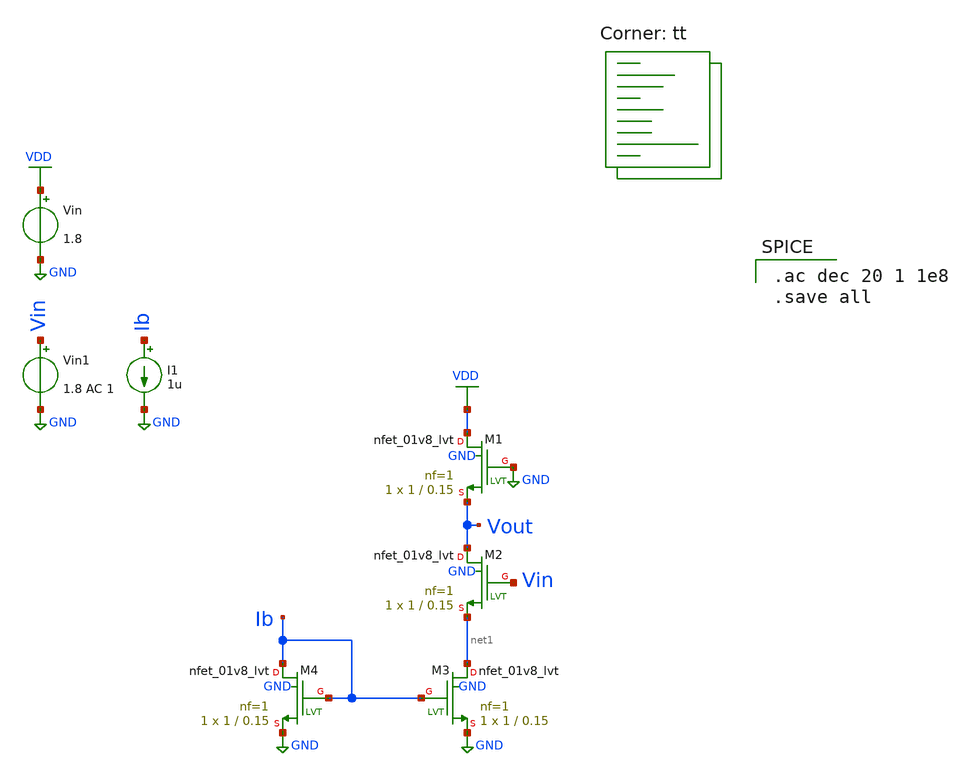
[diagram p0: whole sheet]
** sch_path: xschem/fvf_tb_loop.sch
**.subckt fvf_tb_loop
Vin VDD GND 1.8
Vin1 Vin GND 1.8 AC 1
I1 Ib GND 1u
XM1 VDD GND Vout GND sky130_fd_pr__nfet_01v8_lvt L=0.15 W=1 nf=1 ad='int((nf+1)/2) * W/nf * 0.29' as='int((nf+2)/2) * W/nf * 0.29'
+ pd='2*int((nf+1)/2) * (W/nf + 0.29)' ps='2*int((nf+2)/2) * (W/nf + 0.29)' nrd='0.29 / W' nrs='0.29 / W'
+ sa=0 sb=0 sd=0 mult=1 m=1
XM2 Vout Vin net1 GND sky130_fd_pr__nfet_01v8_lvt L=0.15 W=1 nf=1 ad='int((nf+1)/2) * W/nf * 0.29' as='int((nf+2)/2) * W/nf * 0.29'
+ pd='2*int((nf+1)/2) * (W/nf + 0.29)' ps='2*int((nf+2)/2) * (W/nf + 0.29)' nrd='0.29 / W' nrs='0.29 / W'
+ sa=0 sb=0 sd=0 mult=1 m=1
XM3 net1 Ib GND GND sky130_fd_pr__nfet_01v8_lvt L=0.15 W=1 nf=1 ad='int((nf+1)/2) * W/nf * 0.29' as='int((nf+2)/2) * W/nf * 0.29'
+ pd='2*int((nf+1)/2) * (W/nf + 0.29)' ps='2*int((nf+2)/2) * (W/nf + 0.29)' nrd='0.29 / W' nrs='0.29 / W'
+ sa=0 sb=0 sd=0 mult=1 m=1
XM4 Ib Ib GND GND sky130_fd_pr__nfet_01v8_lvt L=0.15 W=1 nf=1 ad='int((nf+1)/2) * W/nf * 0.29' as='int((nf+2)/2) * W/nf * 0.29'
+ pd='2*int((nf+1)/2) * (W/nf + 0.29)' ps='2*int((nf+2)/2) * (W/nf + 0.29)' nrd='0.29 / W' nrs='0.29 / W'
+ sa=0 sb=0 sd=0 mult=1 m=1
**** begin user architecture code
.lib $::SKYWATER_MODELS/sky130.lib.spice tt

.ac dec 20 1 1e8
.save all

**** end user architecture code
**.ends
.GLOBAL VDD
.GLOBAL GND
.end
